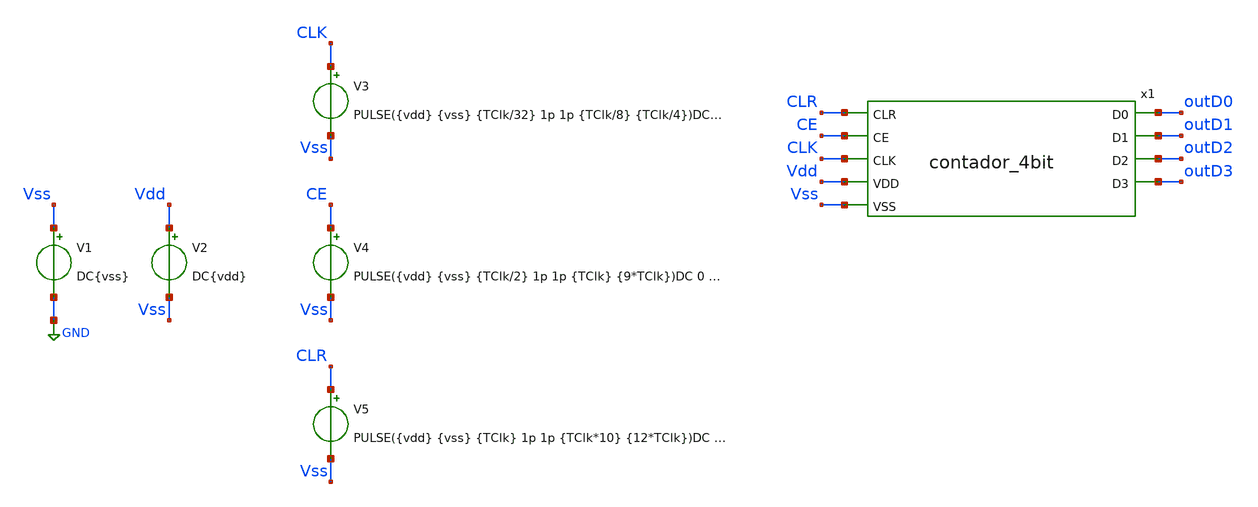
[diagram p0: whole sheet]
** sch_path: icdesign/sch/Contador4bit/tb_contador_4bit.sch
**.subckt tb_contador_4bit
x1 CLR CE CLK outD0 Vdd Vss outD1 outD2 outD3 contador_4bit
V1 Vss GND DC{vss}
V2 Vdd Vss DC{vdd}
V3 CLK Vss PULSE({vdd} {vss} {TClk/32} 1p 1p {TClk/8} {TClk/4})DC 0 AC 0
V4 CE Vss PULSE({vdd} {vss} {TClk/2} 1p 1p {TClk} {9*TClk})DC 0 AC 0
V5 CLR Vss PULSE({vdd} {vss} {TClk} 1p 1p {TClk*10} {12*TClk})DC 0 AC 0
**** begin user architecture code





* Circuit Parameters
.param vdd  = 1.8
.param vss  = 0.0
.param Tclk = 10n
.options TEMP = 65.0


* Include Models
.lib ~/skywater/skywater-pdk/libraries/sky130_fd_pr_ngspice/latest/models/corners/sky130.lib TT


* OP Parameters & Singals to save
.save all


*Simulations
.control
  tran 0.01u 100n
  setplot tran1
  plot v(CLK)v(CLR)+2 v(CE)+4 v(outD0)+6 v(outD1)+8 v(outD2)+10 v(outD3)+12
.endc
.end


**** end user architecture code
**.ends
.GLOBAL GND
.end
